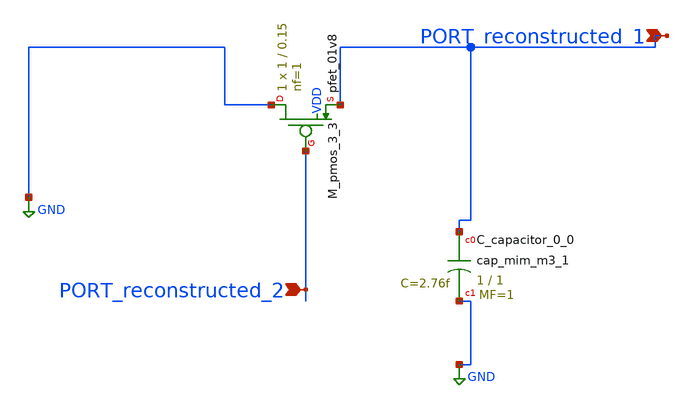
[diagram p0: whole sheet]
** sch_path: schematics/AMSNet/779.sch
**.subckt 779 PORT_reconstructed_1 PORT_reconstructed_2
*.ipin PORT_reconstructed_1
*.ipin PORT_reconstructed_2
XC_capacitor_0_0 PORT_reconstructed_1 GND sky130_fd_pr__cap_mim_m3_1 W=1 L=1 MF=1 m=1
XM_pmos_3_3 GND PORT_reconstructed_2 PORT_reconstructed_1 VDD sky130_fd_pr__pfet_01v8 L=0.15 W=1 nf=1
+ ad='int((1 + 1)/2) * 1 / 1 * 0.29' as='int((1 + 2)/2) * 1 / 1 * 0.29' pd='2*int((1 + 1)/2) * (1 / 1 + 0.29)'
+ ps='2*int((1 + 2)/2) * (1 / 1 + 0.29)' nrd='0.29 / 1 ' nrs='0.29 / 1 ' sa=0 sb=0 sd=0 mult=1 m=1
**.ends
.GLOBAL GND
.end
